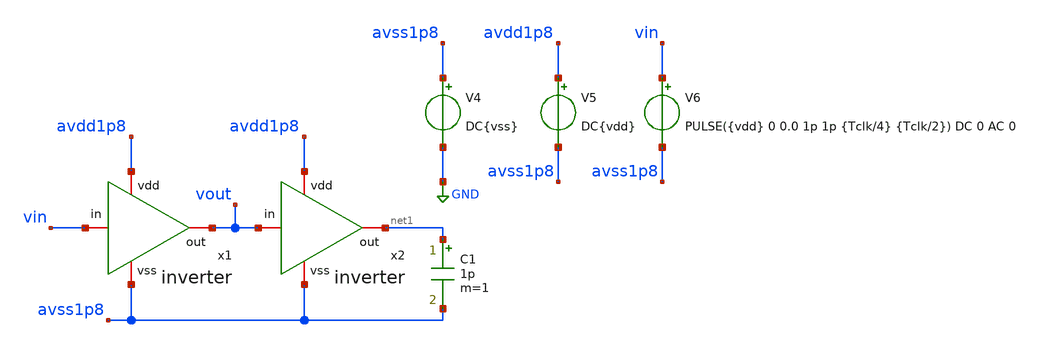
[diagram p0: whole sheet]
** sch_path: verification/testbenches/inverter/tb_inverter.sch
**.subckt tb_inverter
x1 avdd1p8 vout vin avss1p8 inverter
x2 avdd1p8 net1 vout avss1p8 inverter
C1 net1 avss1p8 1p m=1
V4 avss1p8 GND DC{vss}
V5 avdd1p8 avss1p8 DC{vdd}
V6 vin avss1p8 PULSE({vdd} 0 0.0 1p 1p {Tclk/4} {Tclk/2}) DC 0 AC 0
**** begin user architecture code


* Circuit Parameters
.param vdd = 1.2
.param vss = 0.0
.param Tclk = 10n
.options TEMP = 27.0
* Include Models - IHP SG13G2
.lib $PDK_ROOT/sg13g2/libs.tech/ngspice/models/sg13_lv_models.lib typical
* OP Parameters & Singals to save
.save all
*Simulations
.control
tran 0.01u 100n
setplot tran1
plot v(vin) v(vout)+1.2
reset
dc V6 0 1.2 0.01
setplot dc
plot vin vout ylabel vout xlabel vin
set filetype = ascii
write dcsweep.raw
.endc
.end


**** end user architecture code
**.ends

* expanding   symbol:  blocks/inverter/schematic/inverter.sym # of pins=4
** sym_path: blocks/inverter/schematic/inverter.sym
** sch_path: blocks/inverter/schematic/inverter.sch
.subckt inverter vdd out in vss
*.iopin vdd
*.iopin out
*.iopin vss
*.iopin in
XM1 out in vss vss sg13_lv_nmos w=1.0u l=0.13u ng=1 m=1 mm_ok=1
XM2 out in vdd vdd sg13_lv_pmos w=2.0u l=0.13u ng=1 m=1 mm_ok=1
.ends

.GLOBAL GND
.end
